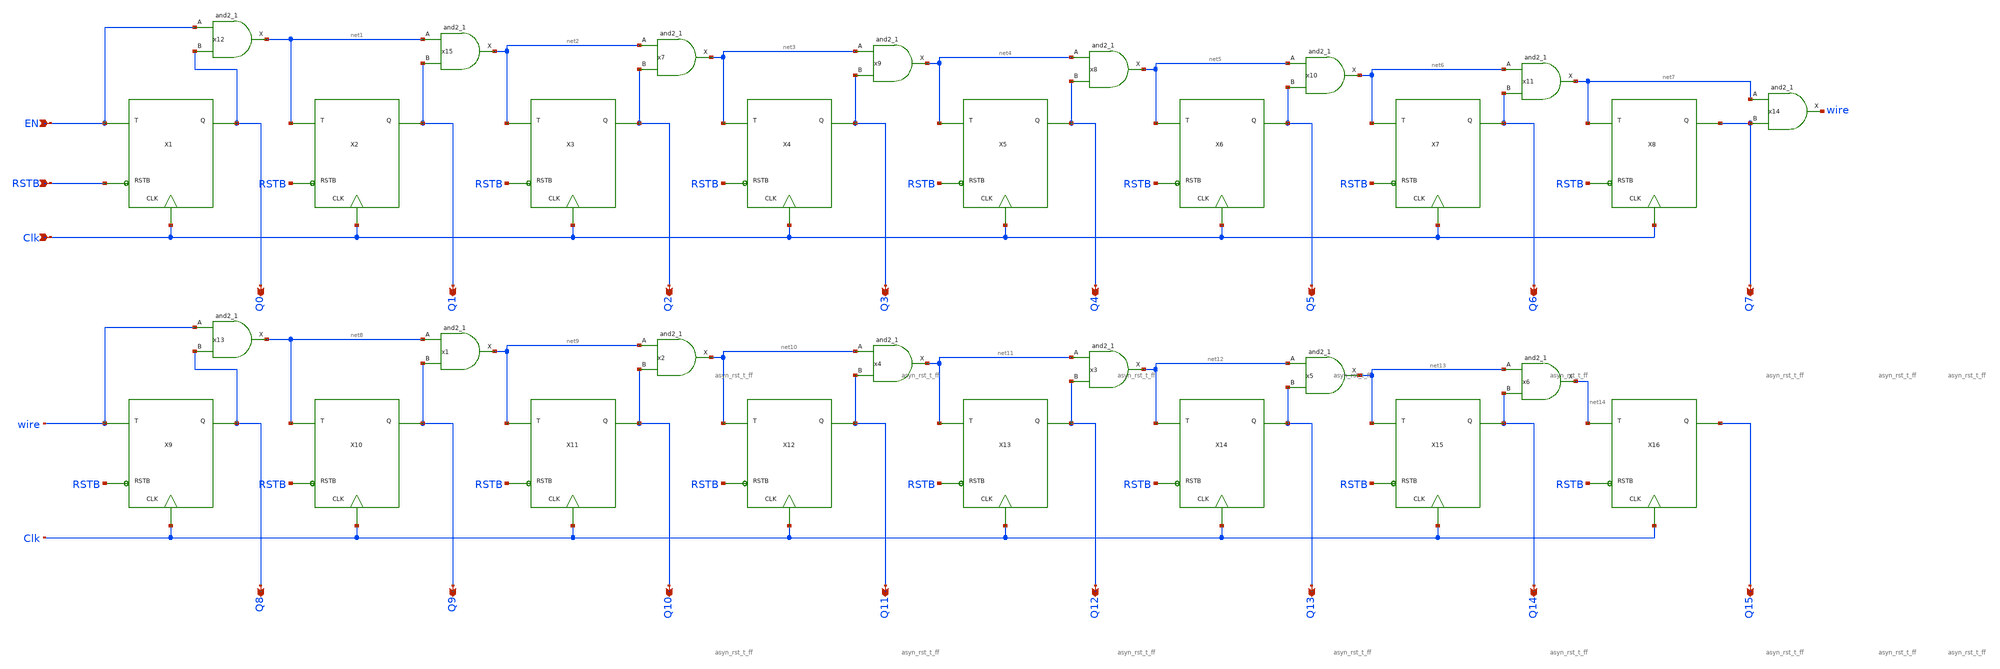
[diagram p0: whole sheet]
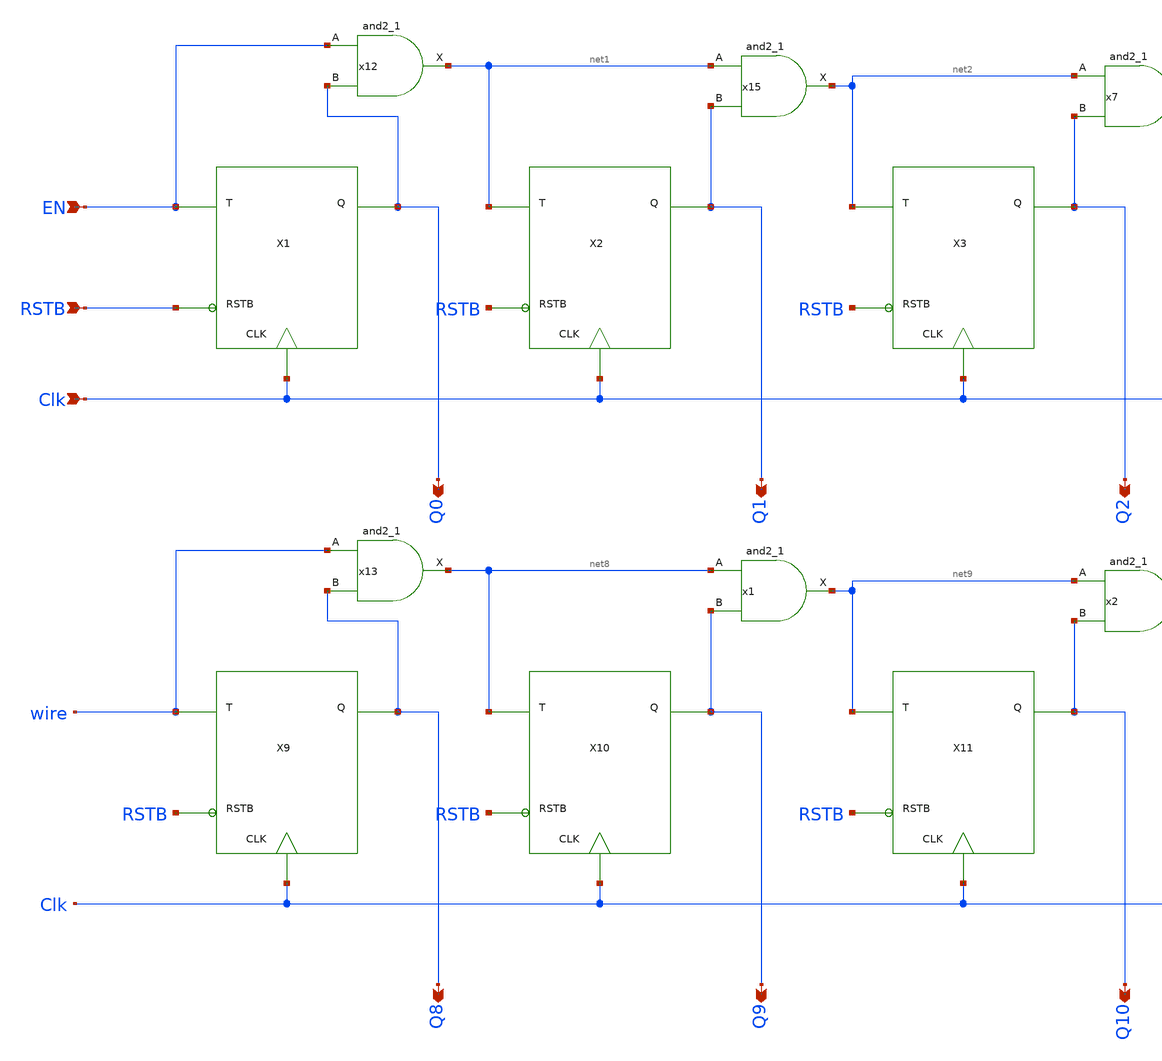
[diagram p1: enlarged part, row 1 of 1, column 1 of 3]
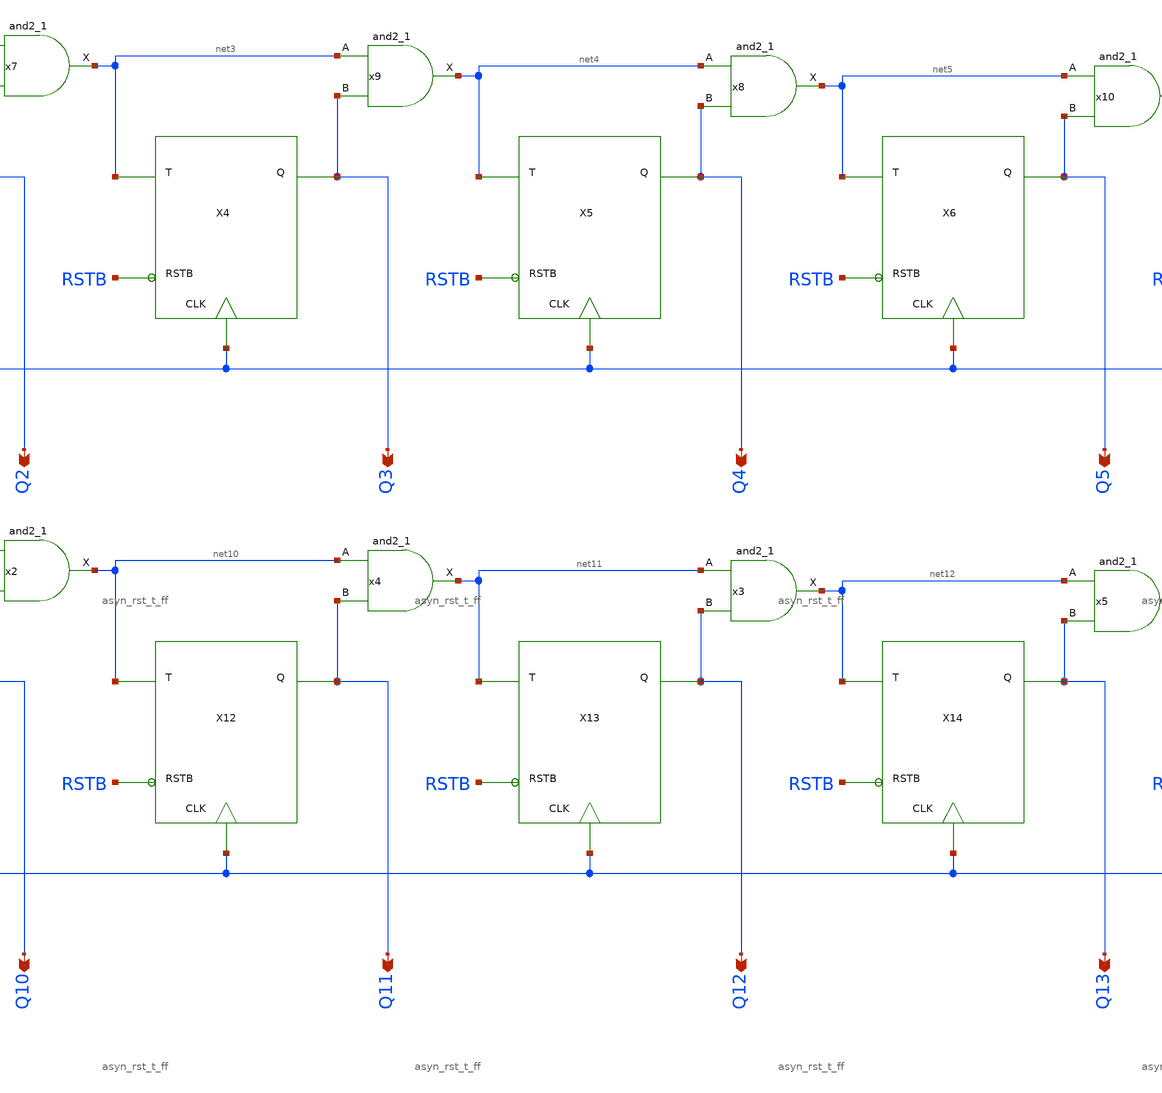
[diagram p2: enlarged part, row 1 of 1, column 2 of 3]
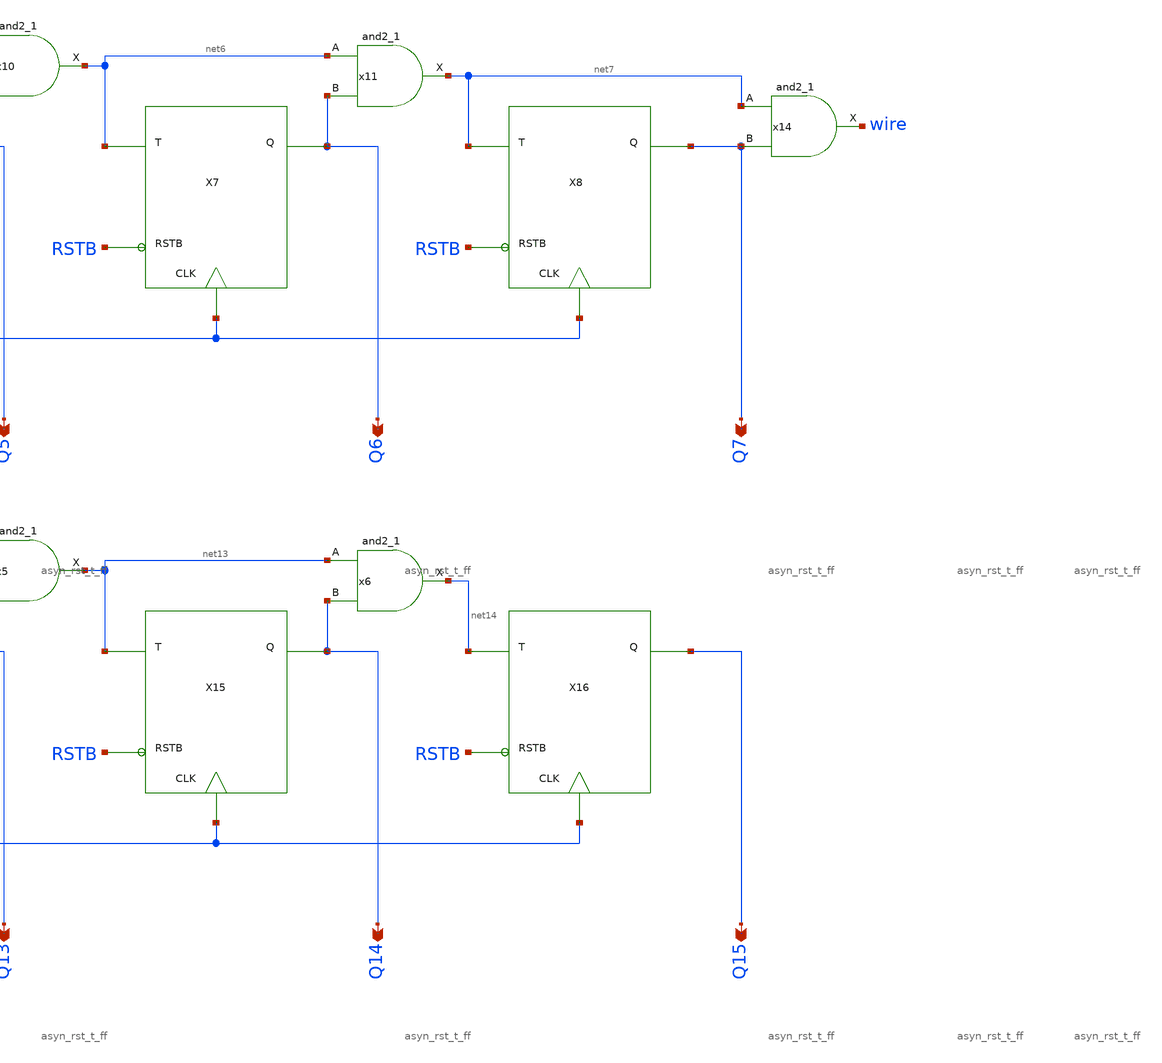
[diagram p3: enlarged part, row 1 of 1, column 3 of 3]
** sch_path: xschem/binary counter/bin_counter.sch
**.subckt bin_counter Clk EN Q0 Q1 Q2 Q4 Q5 Q6 Q7 Q3 Q8 Q9 Q10 Q12 Q13 Q14 Q11 Q15 RSTB
*.ipin Clk
*.ipin EN
*.opin Q0
*.opin Q1
*.opin Q2
*.opin Q4
*.opin Q5
*.opin Q6
*.opin Q7
*.opin Q3
*.opin Q8
*.opin Q9
*.opin Q10
*.opin Q12
*.opin Q13
*.opin Q14
*.opin Q11
*.opin Q15
*.ipin RSTB
x15 net1 Q1 GND GND VDD VDD net2 sky130_fd_sc_lp__and2_1
x7 net2 Q2 GND GND VDD VDD net3 sky130_fd_sc_lp__and2_1
x8 net4 Q4 GND GND VDD VDD net5 sky130_fd_sc_lp__and2_1
x9 net3 Q3 GND GND VDD VDD net4 sky130_fd_sc_lp__and2_1
x10 net5 Q5 GND GND VDD VDD net6 sky130_fd_sc_lp__and2_1
x11 net6 Q6 GND GND VDD VDD net7 sky130_fd_sc_lp__and2_1
x12 EN Q0 GND GND VDD VDD net1 sky130_fd_sc_lp__and2_1
x1 net8 Q9 GND GND VDD VDD net9 sky130_fd_sc_lp__and2_1
x2 net9 Q10 GND GND VDD VDD net10 sky130_fd_sc_lp__and2_1
x3 net11 Q12 GND GND VDD VDD net12 sky130_fd_sc_lp__and2_1
x4 net10 Q11 GND GND VDD VDD net11 sky130_fd_sc_lp__and2_1
x5 net12 Q13 GND GND VDD VDD net13 sky130_fd_sc_lp__and2_1
x6 net13 Q14 GND GND VDD VDD net14 sky130_fd_sc_lp__and2_1
x13 wire Q8 GND GND VDD VDD net8 sky130_fd_sc_lp__and2_1
x14 net7 Q7 GND GND VDD VDD wire sky130_fd_sc_lp__and2_1
X1 EN Q0 Clk RSTB asyn_rst_t_ff
X2 net1 Q1 Clk RSTB asyn_rst_t_ff
X3 net2 Q2 Clk RSTB asyn_rst_t_ff
X4 net3 Q3 Clk RSTB asyn_rst_t_ff
X5 net4 Q4 Clk RSTB asyn_rst_t_ff
X6 net5 Q5 Clk RSTB asyn_rst_t_ff
X7 net6 Q6 Clk RSTB asyn_rst_t_ff
X8 net7 Q7 Clk RSTB asyn_rst_t_ff
X9 wire Q8 Clk RSTB asyn_rst_t_ff
X10 net8 Q9 Clk RSTB asyn_rst_t_ff
X11 net9 Q10 Clk RSTB asyn_rst_t_ff
X12 net10 Q11 Clk RSTB asyn_rst_t_ff
X13 net11 Q12 Clk RSTB asyn_rst_t_ff
X14 net12 Q13 Clk RSTB asyn_rst_t_ff
X15 net13 Q14 Clk RSTB asyn_rst_t_ff
X16 net14 Q15 Clk RSTB asyn_rst_t_ff
**.ends

* expanding   symbol:  T_flip_flop/asyn_rst_t_ff.sym # of pins=4
** sym_path: xschem/T_flip_flop/asyn_rst_t_ff.sym
** sch_path: xschem/T_flip_flop/asyn_rst_t_ff.sch
.subckt asyn_rst_t_ff T Q CLK RSTB
*.ipin T
*.ipin CLK
*.opin Q
*.ipin RSTB
x1 CLK net1 RSTB GND GND VDD VDD Q sky130_fd_sc_lp__dfrtp_1
x3 T Q GND GND VDD VDD net1 sky130_fd_sc_lp__xor2_1
.ends

.end
